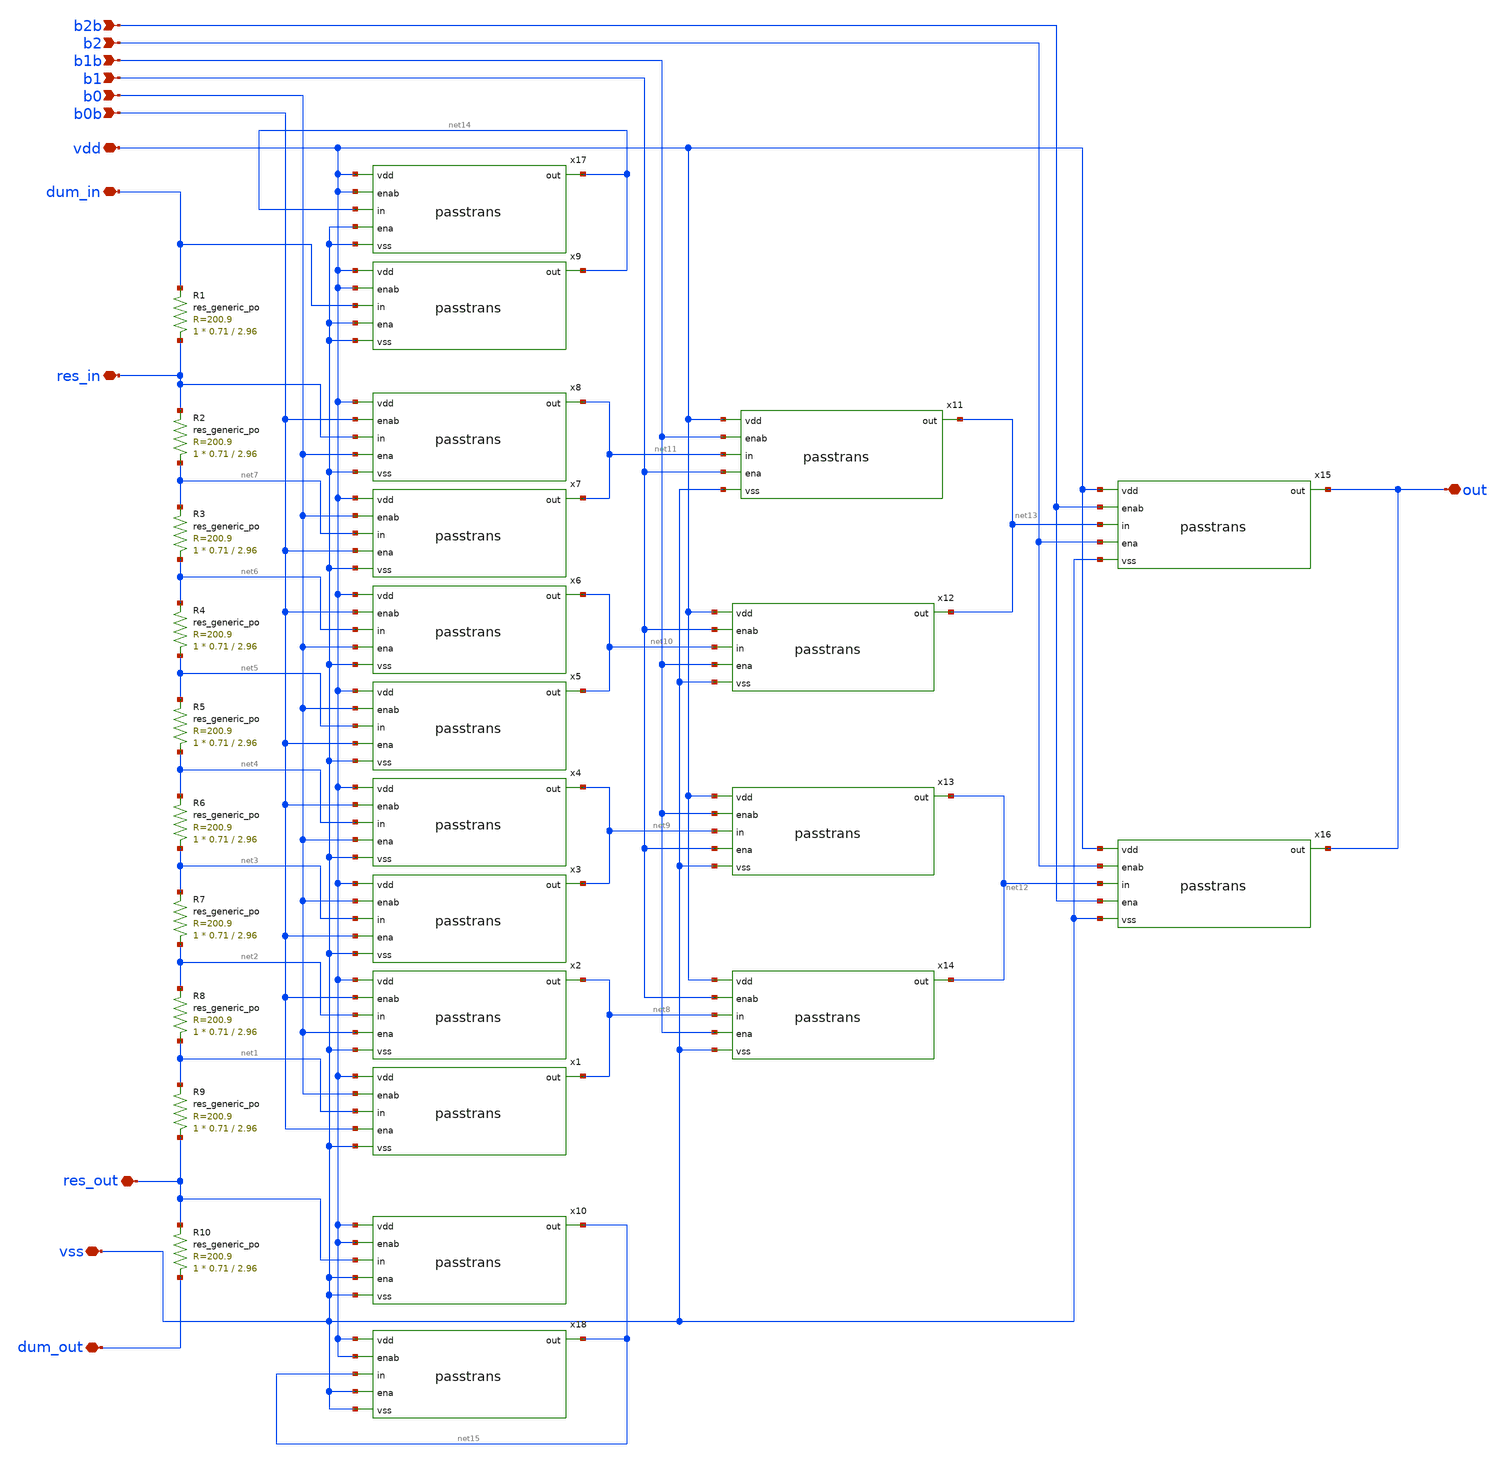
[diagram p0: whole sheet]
** sch_path: xschem/dac_column.sch
**.subckt dac_column res_in vss vdd out b0 b0b b1 b1b b2 b2b dum_in res_out dum_out
*.iopin res_in
*.iopin vss
*.iopin vdd
*.iopin out
*.ipin b0
*.ipin b0b
*.ipin b1
*.ipin b1b
*.ipin b2
*.ipin b2b
*.iopin dum_in
*.iopin res_out
*.iopin dum_out
x1 vdd b0 net8 net1 b0b vss passtrans
x2 vdd b0b net8 net2 b0 vss passtrans
x3 vdd b0 net9 net3 b0b vss passtrans
x4 vdd b0b net9 net4 b0 vss passtrans
x5 vdd b0 net10 net5 b0b vss passtrans
x6 vdd b0b net10 net6 b0 vss passtrans
x7 vdd b0 net11 net7 b0b vss passtrans
x8 vdd b0b net11 res_in b0 vss passtrans
x9 vdd vdd net14 dum_in vss vss passtrans
x10 vdd vdd net15 res_out vss vss passtrans
x11 vdd b1b net13 net11 b1 vss passtrans
x12 vdd b1 net13 net10 b1b vss passtrans
x13 vdd b1b net12 net9 b1 vss passtrans
x14 vdd b1 net12 net8 b1b vss passtrans
x15 vdd b2b out net13 b2 vss passtrans
x16 vdd b2 out net12 b2b vss passtrans
x17 vdd vdd net14 net14 vss vss passtrans
x18 vdd vdd net15 net15 vss vss passtrans
XR1 res_in dum_in sky130_fd_pr__res_generic_po W=0.71 L=2.96 m=1
XR2 net7 res_in sky130_fd_pr__res_generic_po W=0.71 L=2.96 m=1
XR3 net6 net7 sky130_fd_pr__res_generic_po W=0.71 L=2.96 m=1
XR4 net5 net6 sky130_fd_pr__res_generic_po W=0.71 L=2.96 m=1
XR5 net4 net5 sky130_fd_pr__res_generic_po W=0.71 L=2.96 m=1
XR6 net3 net4 sky130_fd_pr__res_generic_po W=0.71 L=2.96 m=1
XR7 net2 net3 sky130_fd_pr__res_generic_po W=0.71 L=2.96 m=1
XR8 net1 net2 sky130_fd_pr__res_generic_po W=0.71 L=2.96 m=1
XR9 res_out net1 sky130_fd_pr__res_generic_po W=0.71 L=2.96 m=1
XR10 dum_out res_out sky130_fd_pr__res_generic_po W=0.71 L=2.96 m=1
**.ends

* expanding   symbol:  passtrans.sym # of pins=6
** sym_path: xschem/passtrans.sym
** sch_path: xschem/passtrans.sch
.subckt passtrans vdd enab out in ena vss
*.ipin enab
*.ipin ena
*.ipin vss
*.ipin vdd
*.iopin in
*.iopin out
XM1 in ena out vss sky130_fd_pr__nfet_g5v0d10v5 L=0.5 W=0.65 nf=1 ad='int((nf+1)/2) * W/nf * 0.29' as='int((nf+2)/2) * W/nf * 0.29'
+ pd='2*int((nf+1)/2) * (W/nf + 0.29)' ps='2*int((nf+2)/2) * (W/nf + 0.29)' nrd='0.29 / W' nrs='0.29 / W'
+ sa=0 sb=0 sd=0 mult=1 m=1
XM2 in enab out vdd sky130_fd_pr__pfet_g5v0d10v5 L=0.5 W=1 nf=1 ad='int((nf+1)/2) * W/nf * 0.29' as='int((nf+2)/2) * W/nf * 0.29'
+ pd='2*int((nf+1)/2) * (W/nf + 0.29)' ps='2*int((nf+2)/2) * (W/nf + 0.29)' nrd='0.29 / W' nrs='0.29 / W'
+ sa=0 sb=0 sd=0 mult=1 m=1
.ends

.end
